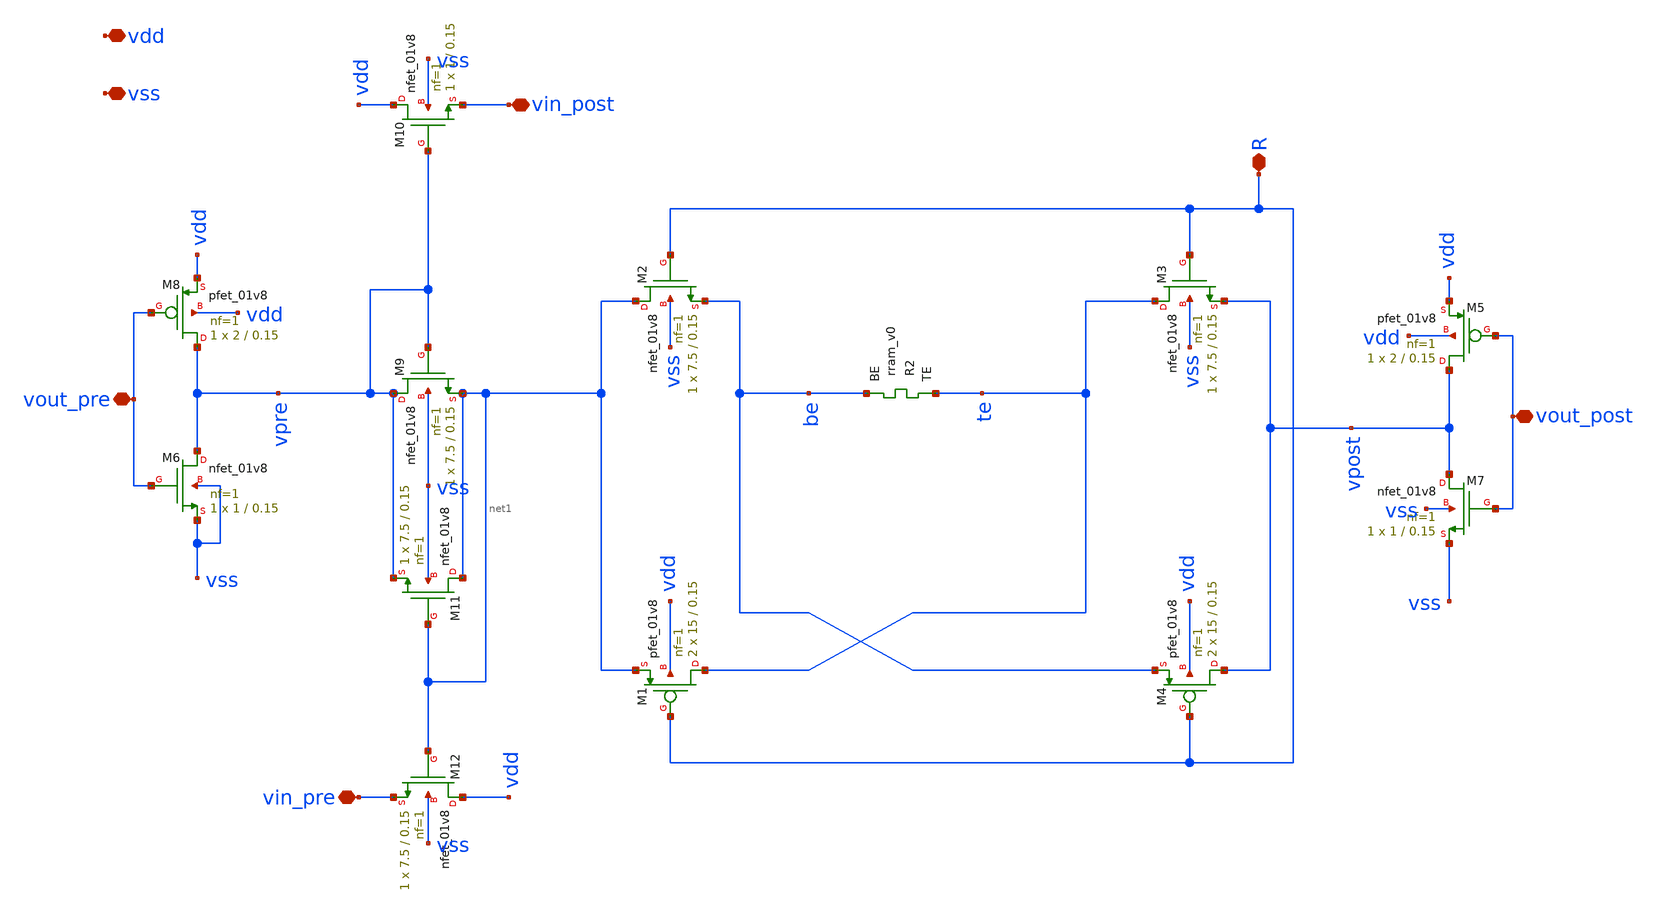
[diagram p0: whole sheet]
** sch_path: Synapse/rstdp_mirror.sch
**.subckt rstdp_mirror vdd vss R vout_post vout_pre vin_post vin_pre
*.iopin vdd
*.iopin vss
*.iopin R
*.iopin vout_post
*.iopin vout_pre
*.iopin vin_post
*.iopin vin_pre
XR2 te be rram_v0
XM2 net1 R be vss sky130_fd_pr__nfet_01v8 L=0.15 W=7.5 nf=1 ad='int((nf+1)/2) * W/nf * 0.29' as='int((nf+2)/2) * W/nf * 0.29'
+ pd='2*int((nf+1)/2) * (W/nf + 0.29)' ps='2*int((nf+2)/2) * (W/nf + 0.29)' nrd='0.29 / W' nrs='0.29 / W'
+ sa=0 sb=0 sd=0 mult=1 m=1
XM3 te R vpost vss sky130_fd_pr__nfet_01v8 L=0.15 W=7.5 nf=1 ad='int((nf+1)/2) * W/nf * 0.29' as='int((nf+2)/2) * W/nf * 0.29'
+ pd='2*int((nf+1)/2) * (W/nf + 0.29)' ps='2*int((nf+2)/2) * (W/nf + 0.29)' nrd='0.29 / W' nrs='0.29 / W'
+ sa=0 sb=0 sd=0 mult=1 m=1
XM1 te R net1 vdd sky130_fd_pr__pfet_01v8 L=0.15 W=15 nf=1 ad='int((nf+1)/2) * W/nf * 0.29' as='int((nf+2)/2) * W/nf * 0.29'
+ pd='2*int((nf+1)/2) * (W/nf + 0.29)' ps='2*int((nf+2)/2) * (W/nf + 0.29)' nrd='0.29 / W' nrs='0.29 / W'
+ sa=0 sb=0 sd=0 mult=2 m=2
XM4 vpost R be vdd sky130_fd_pr__pfet_01v8 L=0.15 W=15 nf=1 ad='int((nf+1)/2) * W/nf * 0.29' as='int((nf+2)/2) * W/nf * 0.29'
+ pd='2*int((nf+1)/2) * (W/nf + 0.29)' ps='2*int((nf+2)/2) * (W/nf + 0.29)' nrd='0.29 / W' nrs='0.29 / W'
+ sa=0 sb=0 sd=0 mult=2 m=2
XM7 vpost vout_post vss vss sky130_fd_pr__nfet_01v8 L=0.15 W=1 nf=1 ad='int((1 + 1)/2) * 1 / 1 * 0.29'
+ as='int((1 + 2)/2) * 1 / 1 * 0.29' pd='2*int((1 + 1)/2) * (1 / 1 + 0.29)' ps='2*int((1 + 2)/2) * (1 / 1 + 0.29)'
+ nrd='0.29 / 1 ' nrs='0.29 / 1 ' sa=0 sb=0 sd=0 mult=1 m=1
XM5 vpost vout_post vdd vdd sky130_fd_pr__pfet_01v8 L=0.15 W=2 nf=1 ad='int((nf+1)/2) * W/nf * 0.29'
+ as='int((nf+2)/2) * W/nf * 0.29' pd='2*int((nf+1)/2) * (W/nf + 0.29)' ps='2*int((nf+2)/2) * (W/nf + 0.29)'
+ nrd='0.29 / W' nrs='0.29 / W' sa=0 sb=0 sd=0 mult=1 m=1
XM6 vpre vout_pre vss vss sky130_fd_pr__nfet_01v8 L=0.15 W=1 nf=1 ad='int((1 + 1)/2) * 1 / 1 * 0.29'
+ as='int((1 + 2)/2) * 1 / 1 * 0.29' pd='2*int((1 + 1)/2) * (1 / 1 + 0.29)' ps='2*int((1 + 2)/2) * (1 / 1 + 0.29)'
+ nrd='0.29 / 1 ' nrs='0.29 / 1 ' sa=0 sb=0 sd=0 mult=1 m=1
XM8 vpre vout_pre vdd vdd sky130_fd_pr__pfet_01v8 L=0.15 W=2 nf=1 ad='int((nf+1)/2) * W/nf * 0.29' as='int((nf+2)/2) * W/nf * 0.29'
+ pd='2*int((nf+1)/2) * (W/nf + 0.29)' ps='2*int((nf+2)/2) * (W/nf + 0.29)' nrd='0.29 / W' nrs='0.29 / W'
+ sa=0 sb=0 sd=0 mult=1 m=1
XM9 vpre vpre net1 vss sky130_fd_pr__nfet_01v8 L=0.15 W=7.5 nf=1 ad='int((1 + 1)/2) * 7.5 / 1 * 0.29'
+ as='int((1 + 2)/2) * 7.5 / 1 * 0.29' pd='2*int((1 + 1)/2) * (7.5 / 1 + 0.29)' ps='2*int((1 + 2)/2) * (7.5 / 1 + 0.29)'
+ nrd='0.29 / 7.5 ' nrs='0.29 / 7.5 ' sa=0 sb=0 sd=0 mult=1 m=1
XM10 vdd vpre vin_post vss sky130_fd_pr__nfet_01v8 L=0.15 W=1 nf=1 ad='int((1 + 1)/2) * 1 / 1 * 0.29'
+ as='int((1 + 2)/2) * 1 / 1 * 0.29' pd='2*int((1 + 1)/2) * (1 / 1 + 0.29)' ps='2*int((1 + 2)/2) * (1 / 1 + 0.29)'
+ nrd='0.29 / 1 ' nrs='0.29 / 1 ' sa=0 sb=0 sd=0 mult=1 m=1
XM11 net1 net1 vpre vss sky130_fd_pr__nfet_01v8 L=0.15 W=7.5 nf=1 ad='int((1 + 1)/2) * 7.5 / 1 * 0.29'
+ as='int((1 + 2)/2) * 7.5 / 1 * 0.29' pd='2*int((1 + 1)/2) * (7.5 / 1 + 0.29)' ps='2*int((1 + 2)/2) * (7.5 / 1 + 0.29)'
+ nrd='0.29 / 7.5 ' nrs='0.29 / 7.5 ' sa=0 sb=0 sd=0 mult=1 m=1
XM12 vdd net1 vin_pre vss sky130_fd_pr__nfet_01v8 L=0.15 W=7.5 nf=1 ad='int((1 + 1)/2) * 7.5 / 1 * 0.29'
+ as='int((1 + 2)/2) * 7.5 / 1 * 0.29' pd='2*int((1 + 1)/2) * (7.5 / 1 + 0.29)' ps='2*int((1 + 2)/2) * (7.5 / 1 + 0.29)'
+ nrd='0.29 / 7.5 ' nrs='0.29 / 7.5 ' sa=0 sb=0 sd=0 mult=1 m=1
**.ends
.end
